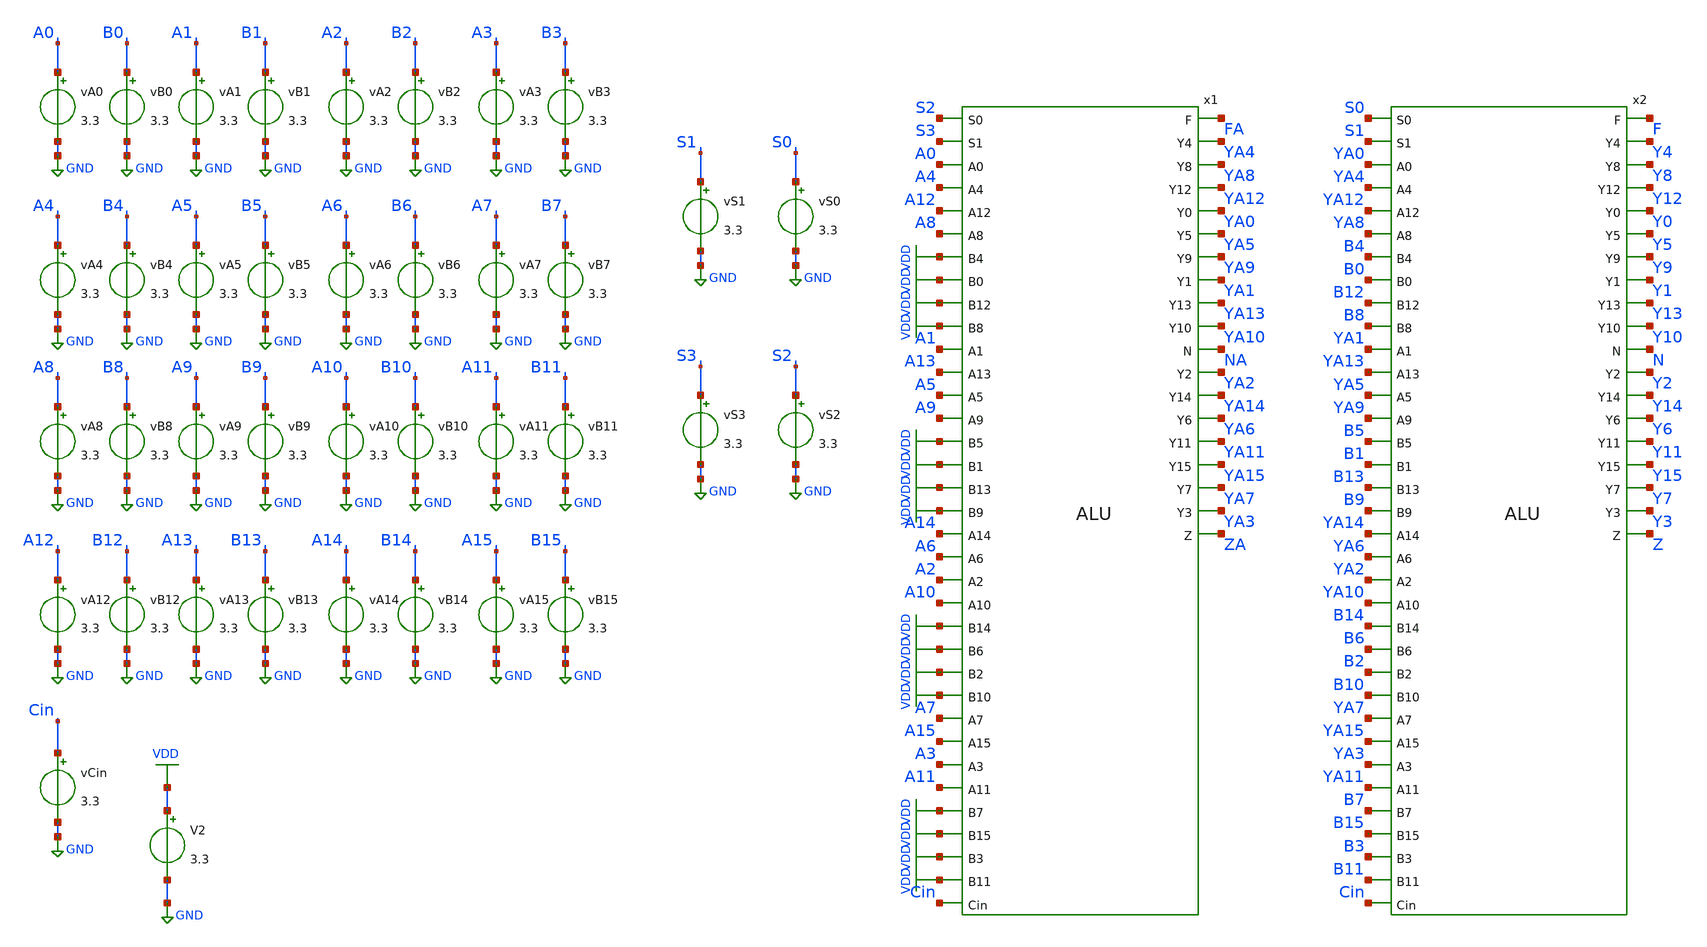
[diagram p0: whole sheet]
** sch_path: tbs/alu_tb_subtract_overflow.sch
**.subckt alu_tb_subtract_overflow
x1 S2 S3 FA A0 A4 A12 A8 VDD VDD VDD VDD A1 A13 A5 A9 YA4 YA8 YA12 YA0 VDD VDD VDD VDD YA5 YA9 YA1
+ YA13 A14 A6 A2 A10 YA10 NA YA2 YA14 YA6 VDD VDD VDD VDD YA11 YA15 YA7 YA3 A7 A15 A3 A11 VDD VDD VDD VDD
+ Cin ZA ALU
vA0 A0 GND 3.3
vB0 B0 GND 3.3
vA1 A1 GND 3.3
vB1 B1 GND 3.3
vA2 A2 GND 3.3
vB2 B2 GND 3.3
vA3 A3 GND 3.3
vB3 B3 GND 3.3
vA4 A4 GND 3.3
vB4 B4 GND 3.3
vA5 A5 GND 3.3
vB5 B5 GND 3.3
vA6 A6 GND 3.3
vB6 B6 GND 3.3
vA7 A7 GND 3.3
vB7 B7 GND 3.3
vA8 A8 GND 3.3
vB8 B8 GND 3.3
vA9 A9 GND 3.3
vB9 B9 GND 3.3
vA10 A10 GND 3.3
vB10 B10 GND 3.3
vA11 A11 GND 3.3
vB11 B11 GND 3.3
vA12 A12 GND 3.3
vB12 B12 GND 3.3
vA13 A13 GND 3.3
vB13 B13 GND 3.3
vA14 A14 GND 3.3
vB14 B14 GND 3.3
vA15 A15 GND 3.3
vB15 B15 GND 3.3
vS0 S0 GND 3.3
vS1 S1 GND 3.3
vCin Cin GND 3.3
V2 VDD GND 3.3
x2 S0 S1 F YA0 YA4 YA12 YA8 B4 B0 B12 B8 YA1 YA13 YA5 YA9 Y4 Y8 Y12 Y0 B5 B1 B13 B9 Y5 Y9 Y1 Y13
+ YA14 YA6 YA2 YA10 Y10 N Y2 Y14 Y6 B14 B6 B2 B10 Y11 Y15 Y7 Y3 YA7 YA15 YA3 YA11 B7 B15 B3 B11 Cin Z ALU
vS2 S2 GND 3.3
vS3 S3 GND 3.3
**** begin user architecture code


.control
  let vlow = 0
  let vhigh = 3.3

  * ADD mode
  alter VS1 = $&vlow
  alter VS0 = $&vlow
  alter VS3 = $&vhigh
  alter VS2 = $&vhigh

  * Carry in = 0
  alter VCin = $&vhigh
* This does B-A
* --- A = 0x0001 (All bits High) ---
  alter VA15 = $&vlow
  alter VA14 = $&vlow
  alter VA13 = $&vlow
  alter VA12 = $&vlow
  alter VA11 = $&vlow
  alter VA10 = $&vlow
  alter VA9  = $&vlow
  alter VA8  = $&vlow
  alter VA7  = $&vlow
  alter VA6  = $&vlow
  alter VA5  = $&vlow
  alter VA4  = $&vlow
  alter VA3  = $&vlow
  alter VA2  = $&vlow
  alter VA1  = $&vlow
  alter VA0  = $&vhigh

  * --- B = 0x0000 (Only Bit 0 High) ---
  alter VB15 = $&vlow
  alter VB14 = $&vlow
  alter VB13 = $&vlow
  alter VB12 = $&vlow
  alter VB11 = $&vlow
  alter VB10 = $&vlow
  alter VB9  = $&vlow
  alter VB8  = $&vlow
  alter VB7  = $&vlow
  alter VB6  = $&vlow
  alter VB5  = $&vlow
  alter VB4  = $&vlow
  alter VB3  = $&vlow
  alter VB2  = $&vlow
  alter VB1  = $&vlow
  alter VB0  = $&vlow

  * Solve DC operating point first
  op
display v(y0) v(y1) v(y2)

  * Print only the bits that matter for 3 + 5 = 8
  * Optional very short transient, just for waveform screenshot
  tran 0.1n 30n
print v(y3)[307] v(y2)[307] v(y1)[307] v(y0)[307]
let last = length(v(y0)) - 1

  * --- Digitizing each bit (1 if > 3V, else 0) ---
meas tran v0  find v(y0)  at=30n
  meas tran v1  find v(y1)  at=30n
  meas tran v2  find v(y2)  at=30n
  meas tran v3  find v(y3)  at=30n
  meas tran v4  find v(y4)  at=30n
  meas tran v5  find v(y5)  at=30n
  meas tran v6  find v(y6)  at=30n
  meas tran v7  find v(y7)  at=30n
  meas tran v8  find v(y8)  at=30n
  meas tran v9  find v(y9)  at=30n
  meas tran v10 find v(y10) at=30n
  meas tran v11 find v(y11) at=30n
  meas tran v12 find v(y12) at=30n
  meas tran v13 find v(y13) at=30n
  meas tran v14 find v(y14) at=30n
  meas tran v15 find v(y15) at=30n

  * 2. Initialize our tracking variables
  let decimal_result = 0
  let b0=0 b1=0 b2=0 b3=0 b4=0 b5=0 b6=0 b7=0
  let b8=0 b9=0 b10=0 b11=0 b12=0 b13=0 b14=0 b15=0

  * 3. Logic checks using IF blocks (Standard threshold 1.6V)
  if v0 > 1.6
    let b0 = 1
    let decimal_result = decimal_result + 1
  end
  if v1 > 1.6
    let b1 = 1
    let decimal_result = decimal_result + 2
  end
  if v2 > 1.6
    let b2 = 1
    let decimal_result = decimal_result + 4
  end
  if v3 > 1.6
    let b3 = 1
    let decimal_result = decimal_result + 8
  end
  if v4 > 1.6
    let b4 = 1
    let decimal_result = decimal_result + 16
  end
  if v5 > 1.6
    let b5 = 1
    let decimal_result = decimal_result + 32
  end
  if v6 > 1.6
    let b6 = 1
    let decimal_result = decimal_result + 64
  end
  if v7 > 1.6
    let b7 = 1
    let decimal_result = decimal_result + 128
  end
  if v8 > 1.6
    let b8 = 1
    let decimal_result = decimal_result + 256
  end
  if v9 > 1.6
    let b9 = 1
    let decimal_result = decimal_result + 512
  end
  if v10 > 1.6
    let b10 = 1
    let decimal_result = decimal_result + 1024
  end
  if v11 > 1.6
    let b11 = 1
    let decimal_result = decimal_result + 2048
  end
  if v12 > 1.6
    let b12 = 1
    let decimal_result = decimal_result + 4096
  end
  if v13 > 1.6
    let b13 = 1
    let decimal_result = decimal_result + 8192
  end
  if v14 > 1.6
    let b14 = 1
    let decimal_result = decimal_result + 16384
  end
  if v15 > 1.6
    let b15 = 1
    let decimal_result = decimal_result + 32768
  end
  * --- Calculate Decimal Sum ---
echo subtracting 1 from 0 should give all 1s:
print decimal_result
print F[100]
print v15
write alu_add_results.raw
.endc



.include $::180MCU_MODELS/design.ngspice
.lib $::180MCU_MODELS/sm141064.ngspice typical

**** end user architecture code
**.ends
.GLOBAL GND
.GLOBAL VDD
.end
